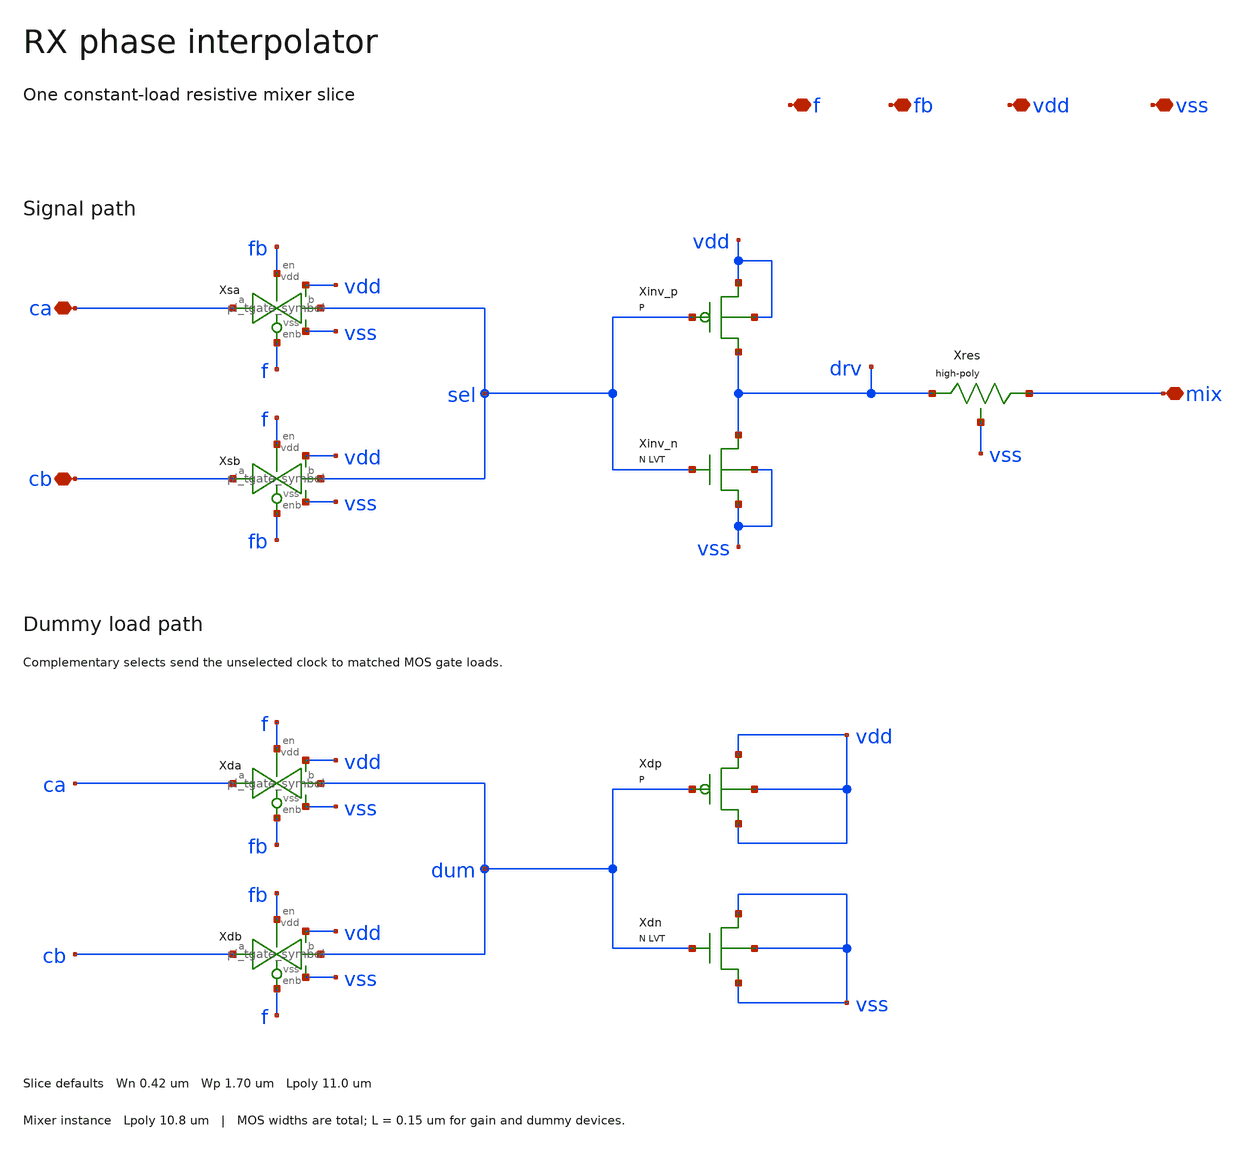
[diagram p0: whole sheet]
** sch_path: analog/rx/cmos_rx/schematic/pi_slice_r.sch
**.subckt pi_slice_r ca cb f fb mix vdd vss
*.iopin ca
*.iopin cb
*.iopin f
*.iopin fb
*.iopin mix
*.iopin vdd
*.iopin vss
Xsa ca sel fb f vdd vss pi_tgate_lvt wn=0.42 wp=0.75 nfn=1 nfp=1
Xsb cb sel f fb vdd vss pi_tgate_lvt wn=0.42 wp=0.75 nfn=1 nfp=1
Xinv_p drv sel vdd vdd serdes_pfet w={wp} l=0.15 nf=1
Xinv_n drv sel vss vss serdes_nfet_lvt w={wn} l=0.15 nf=1
Xres drv mix vss sky130_fd_pr__res_high_po_0p69 l={lres}
Xda ca dum f fb vdd vss pi_tgate_lvt wn=0.42 wp=0.75 nfn=1 nfp=1
Xdb cb dum fb f vdd vss pi_tgate_lvt wn=0.42 wp=0.75 nfn=1 nfp=1
Xdp vdd dum vdd vdd serdes_pfet w={wp} l=0.15 nf=1
Xdn vss dum vss vss serdes_nfet_lvt w={wn} l=0.15 nf=1
**.ends
.end
